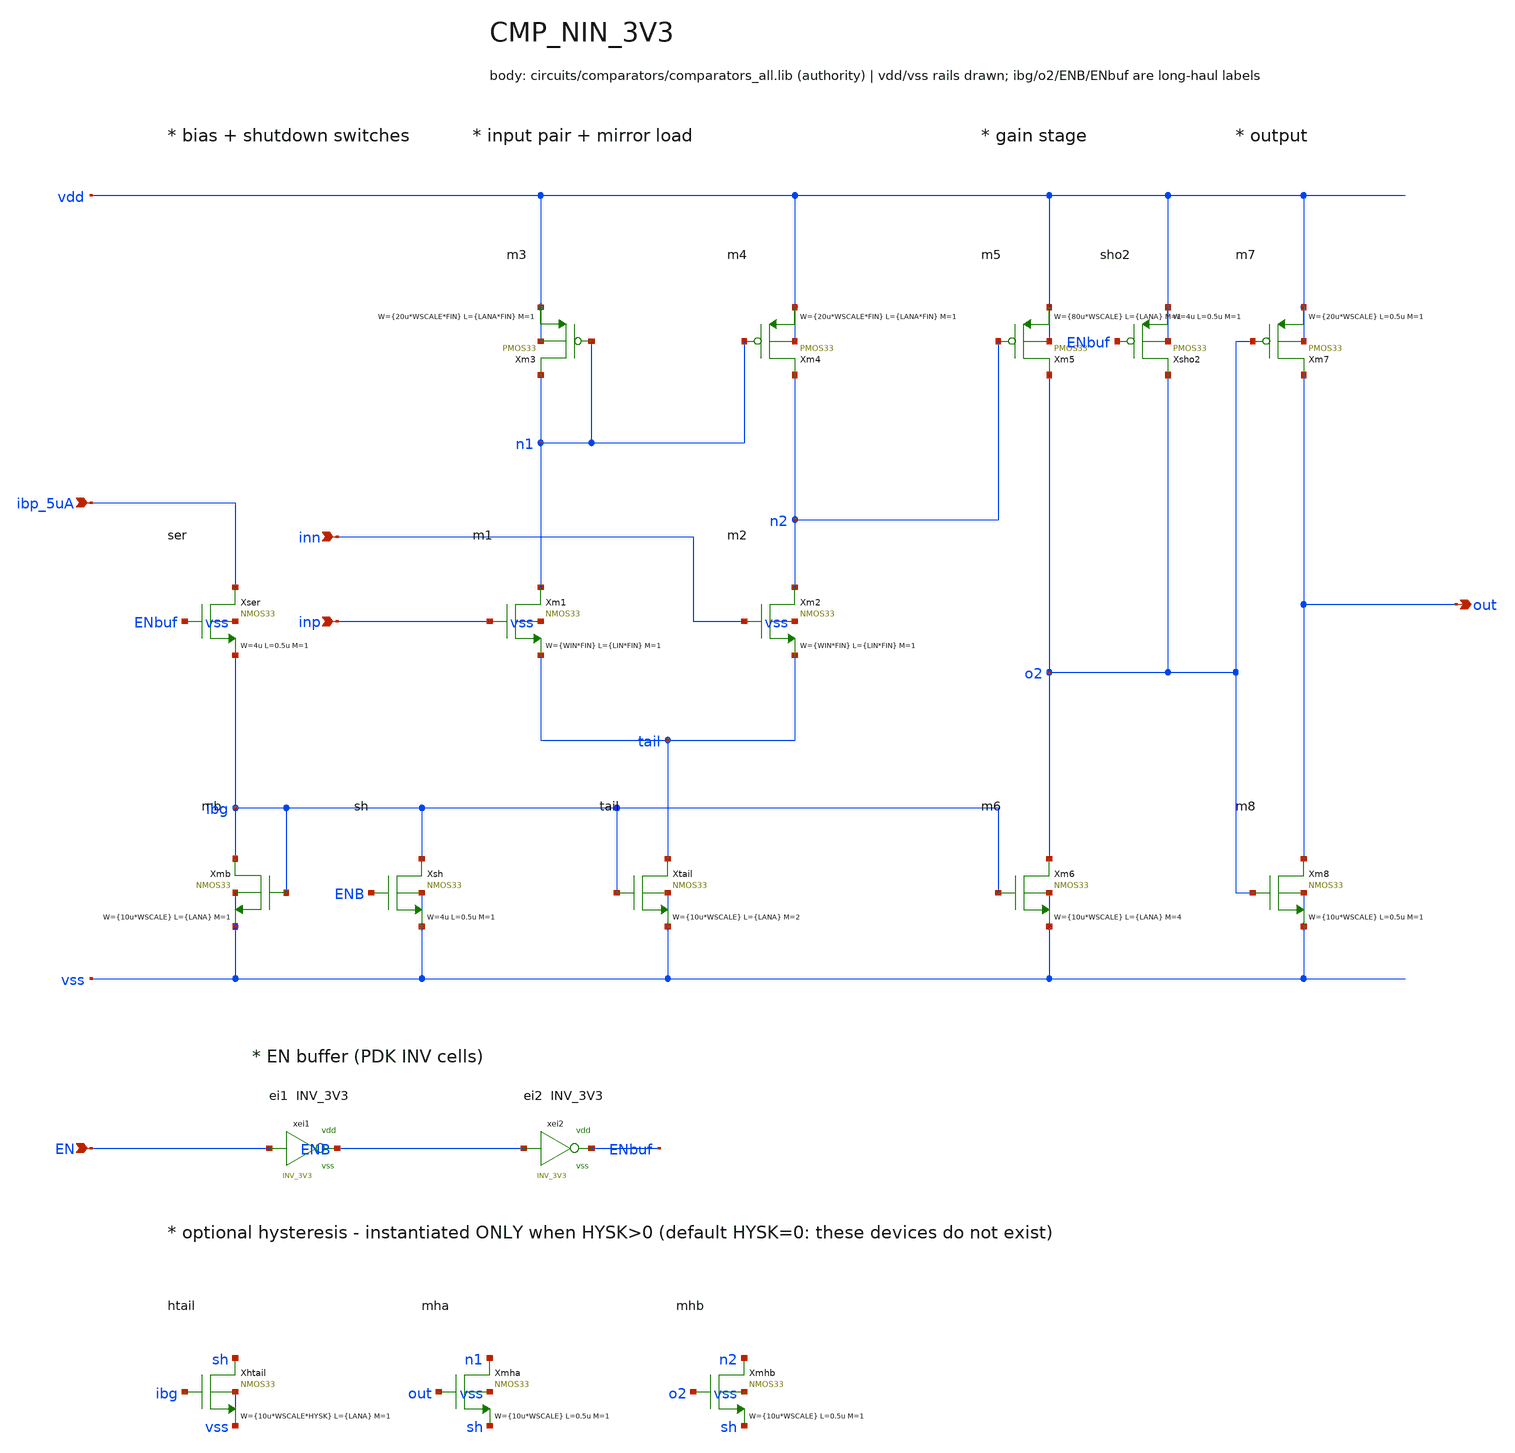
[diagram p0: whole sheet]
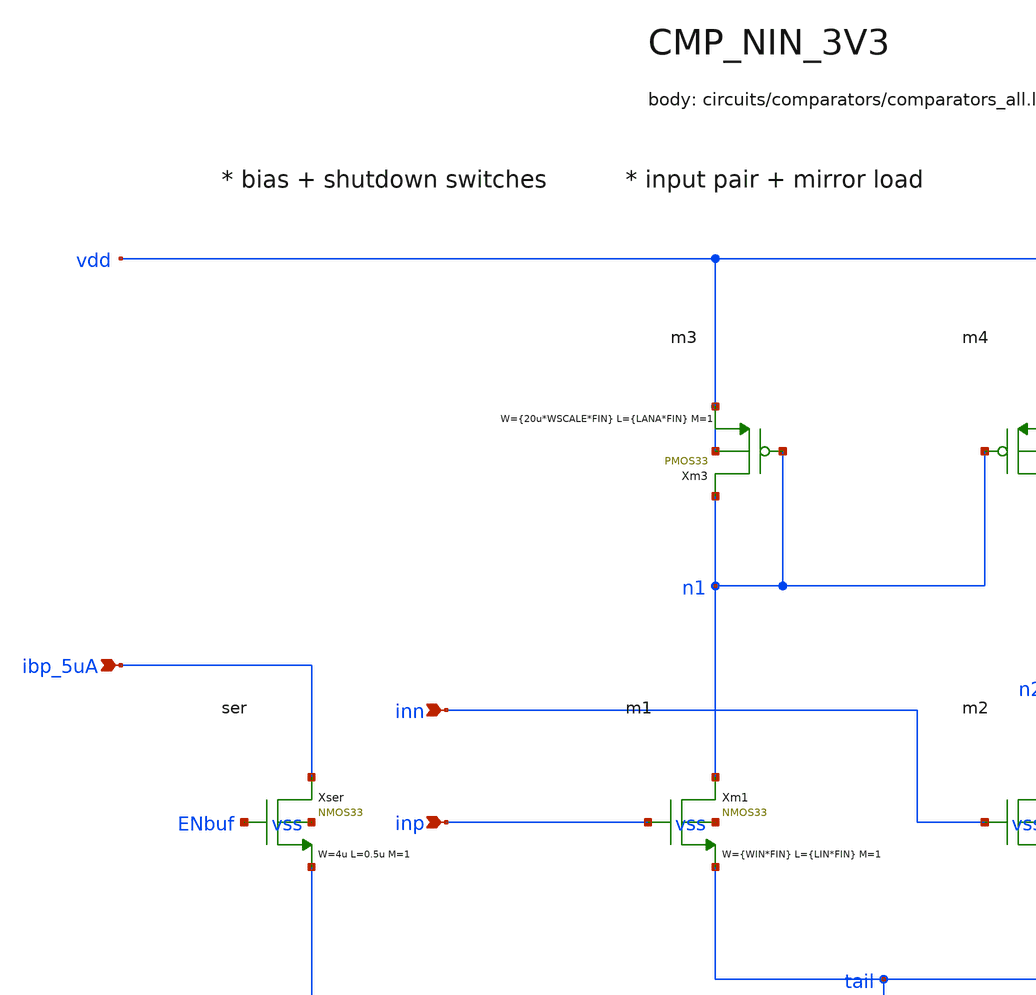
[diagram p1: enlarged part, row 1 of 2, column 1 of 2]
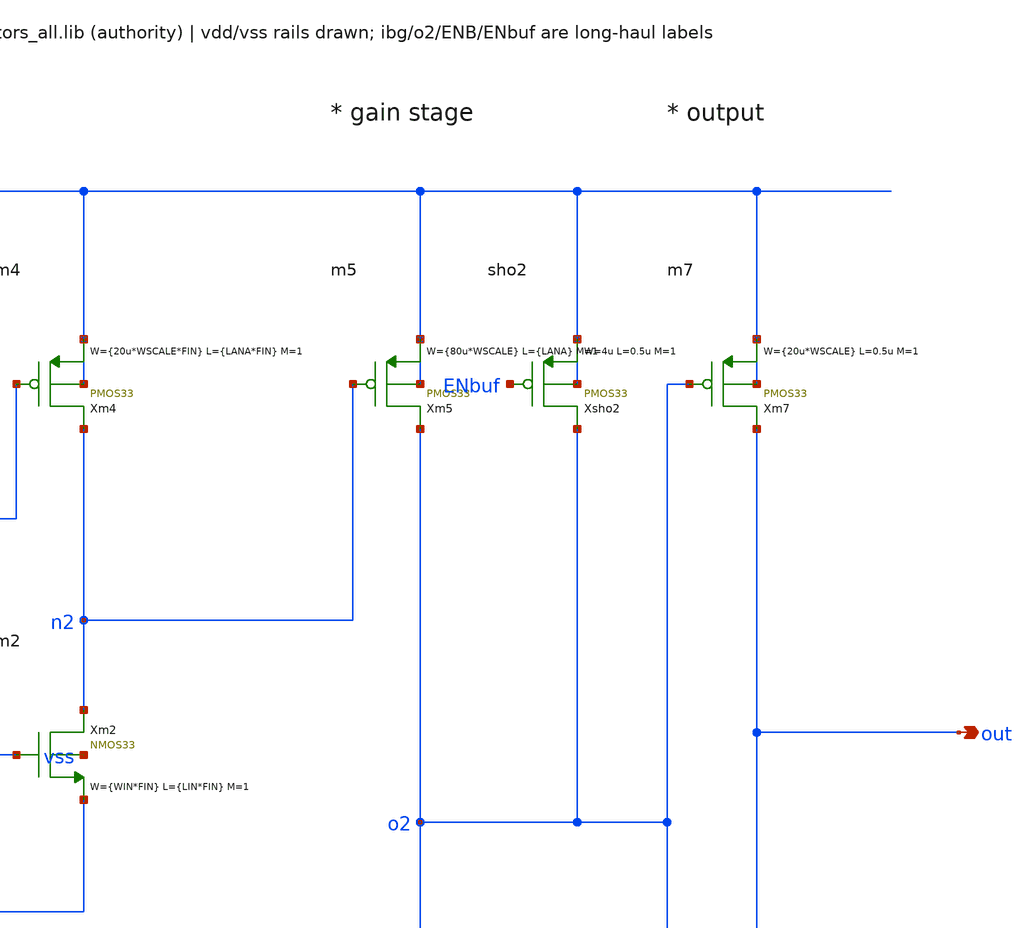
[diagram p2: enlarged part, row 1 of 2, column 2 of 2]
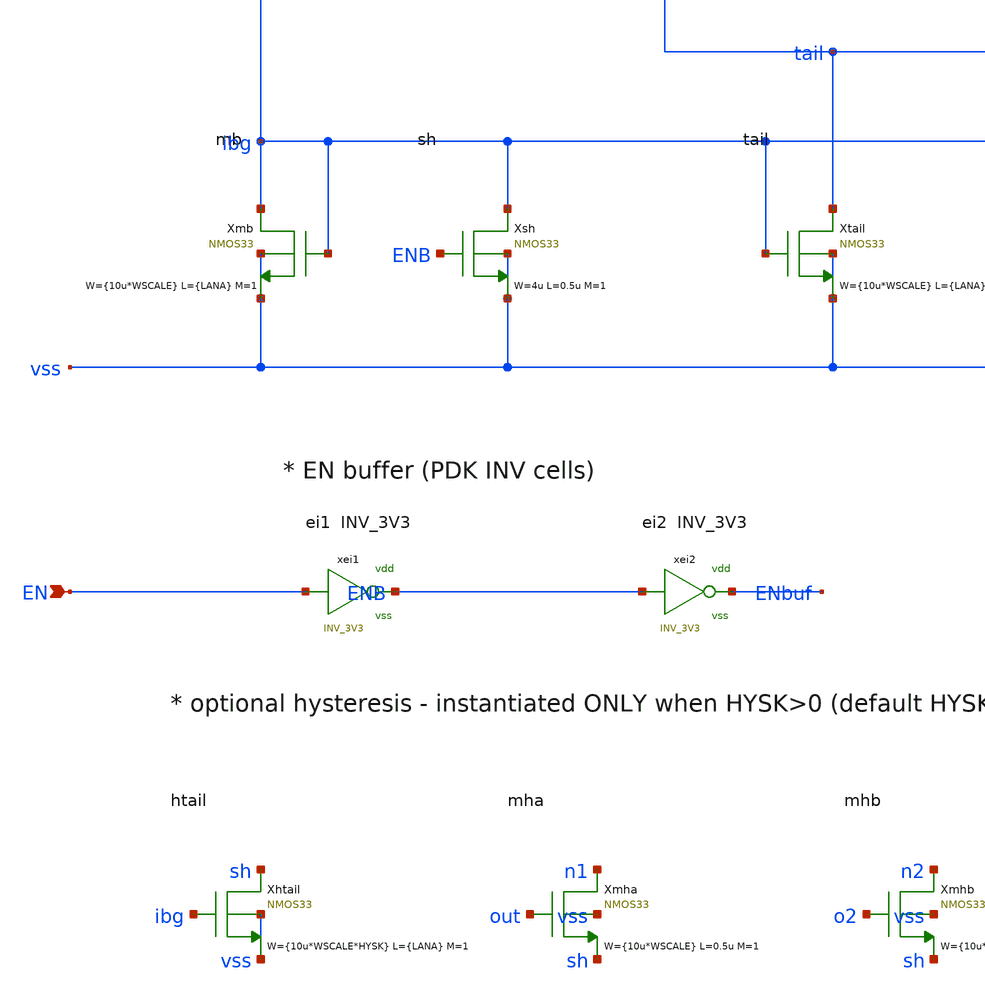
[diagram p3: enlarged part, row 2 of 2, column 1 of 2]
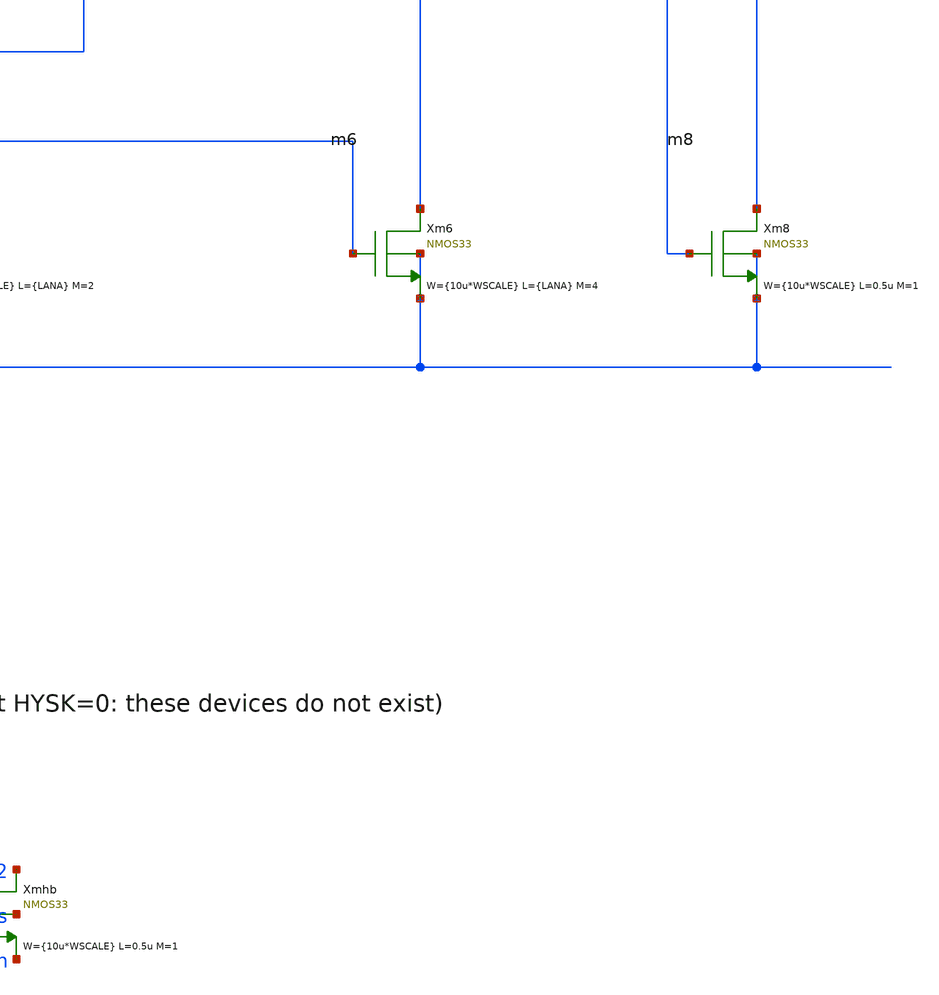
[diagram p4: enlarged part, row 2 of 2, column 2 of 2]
** sch_path: xschem/comparators/CMP_NIN_3V3.sch
**.subckt CMP_NIN_3V3 ibp_5uA out inp inn EN
*.ipin ibp_5uA
*.opin out
*.ipin inp
*.ipin inn
*.ipin EN
Xmb ibg ibg vss vss NMOS33 W={10u*WSCALE} L={LANA} M=1 MM_SIGMA=0
Xtail tail ibg vss vss NMOS33 W={10u*WSCALE} L={LANA} M=2 MM_SIGMA=0
Xm1 n1 inp tail vss NMOS33 W={WIN*FIN} L={LIN*FIN} M=1 MM_SIGMA=0
Xm2 n2 inn tail vss NMOS33 W={WIN*FIN} L={LIN*FIN} M=1 MM_SIGMA=0
Xm3 n1 n1 vdd vdd PMOS33 W={20u*WSCALE*FIN} L={LANA*FIN} M=1 MM_SIGMA=0
Xm4 n2 n1 vdd vdd PMOS33 W={20u*WSCALE*FIN} L={LANA*FIN} M=1 MM_SIGMA=0
Xm5 o2 n2 vdd vdd PMOS33 W={80u*WSCALE} L={LANA} M=1 MM_SIGMA=0
Xm6 o2 ibg vss vss NMOS33 W={10u*WSCALE} L={LANA} M=4 MM_SIGMA=0
Xm7 out o2 vdd vdd PMOS33 W={20u*WSCALE} L=0.5u M=1 MM_SIGMA=0
Xm8 out o2 vss vss NMOS33 W={10u*WSCALE} L=0.5u M=1 MM_SIGMA=0
xei1 EN ENB vdd vss INV_3V3
xei2 ENB ENbuf vdd vss INV_3V3
Xsh ibg ENB vss vss NMOS33 W=4u L=0.5u M=1 MM_SIGMA=0
Xsho2 o2 ENbuf vdd vdd PMOS33 W=4u L=0.5u M=1 MM_SIGMA=0
Xser ibp_5uA ENbuf ibg vss NMOS33 W=4u L=0.5u M=1 MM_SIGMA=0
Xhtail sh ibg vss vss NMOS33 W={10u*WSCALE*HYSK} L={LANA} M=1 MM_SIGMA=0
Xmha n1 out sh vss NMOS33 W={10u*WSCALE} L=0.5u M=1 MM_SIGMA=0
Xmhb n2 o2 sh vss NMOS33 W={10u*WSCALE} L=0.5u M=1 MM_SIGMA=0
**.ends

* expanding   symbol:  logic/INV_3V3.sym # of pins=2
** sym_path: xschem/logic/INV_3V3.sym
* INV_3V3 body is defined in circuits/async_logic_design/cells.lib
.end
